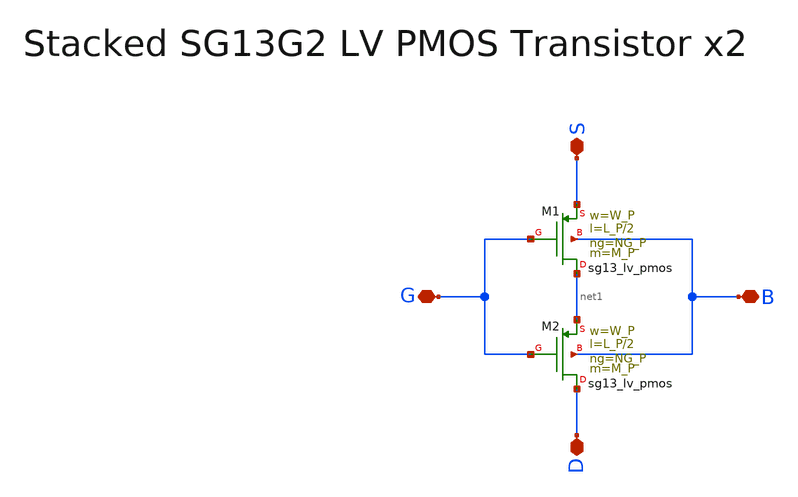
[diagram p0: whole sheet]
** sch_path: SG13G2_ATBS-ADC-main/xschem/stacked_transistors/sg13g2_lv_pmos_stacked/sg13g2_lv_pmos_stacked_x2.sch
**.subckt sg13g2_lv_pmos_stacked_x2 D S G B
*.iopin D
*.iopin S
*.iopin G
*.iopin B
XM1 net1 G S B sg13_lv_pmos w=W_P l=L_P/2 ng=NG_P m=M_P mm_ok=1
XM2 D G net1 B sg13_lv_pmos w=W_P l=L_P/2 ng=NG_P m=M_P mm_ok=1
**.ends
.end
